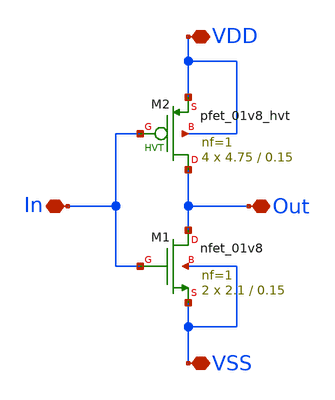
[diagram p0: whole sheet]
** sch_path: HVT/inverter/inverter.sch
**.subckt inverter VDD Out VSS In
*.iopin VDD
*.iopin Out
*.iopin VSS
*.iopin In
XM2 Out In VDD VDD sky130_fd_pr__pfet_01v8_hvt L=0.15 W=4.75 nf=1 ad='int((nf+1)/2) * W/nf * 0.29' as='int((nf+2)/2) * W/nf * 0.29'
+ pd='2*int((nf+1)/2) * (W/nf + 0.29)' ps='2*int((nf+2)/2) * (W/nf + 0.29)' nrd='0.29 / W' nrs='0.29 / W'
+ sa=0 sb=0 sd=0 mult=4 m=4
XM1 Out In VSS VSS sky130_fd_pr__nfet_01v8 L=0.15 W=2.1 nf=1 ad='int((nf+1)/2) * W/nf * 0.29' as='int((nf+2)/2) * W/nf * 0.29'
+ pd='2*int((nf+1)/2) * (W/nf + 0.29)' ps='2*int((nf+2)/2) * (W/nf + 0.29)' nrd='0.29 / W' nrs='0.29 / W'
+ sa=0 sb=0 sd=0 mult=2 m=2
**.ends
.end
